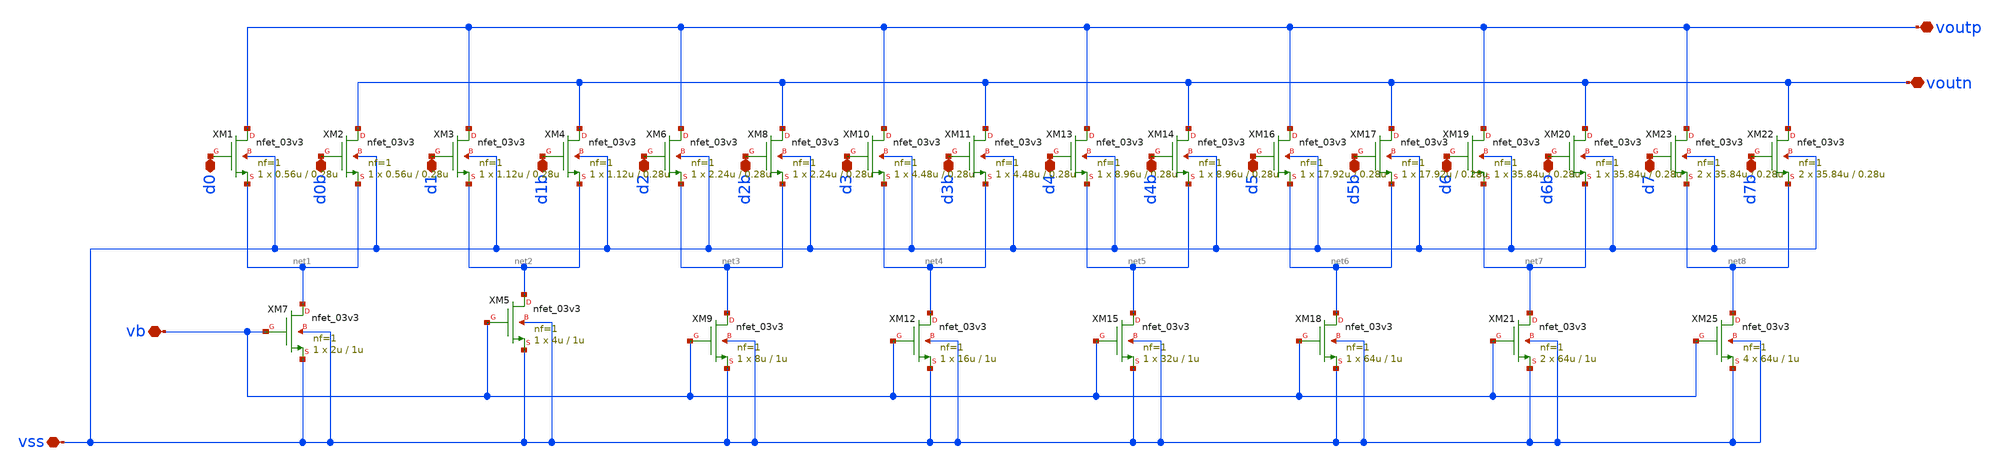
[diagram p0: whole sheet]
** sch_path: analog/dac/current_steering_dac.sch
**.subckt current_steering_dac voutp voutn d7b d7 d6b d6 d5b d5 d4b d4 d3b d3 d2b d2 d1b d1 d0b d0
*+ vb vss
*.iopin voutp
*.iopin voutn
*.iopin d7b
*.iopin d7
*.iopin d6b
*.iopin d6
*.iopin d5b
*.iopin d5
*.iopin d4b
*.iopin d4
*.iopin d3b
*.iopin d3
*.iopin d2b
*.iopin d2
*.iopin d1b
*.iopin d1
*.iopin d0b
*.iopin d0
*.iopin vb
*.iopin vss
XM1 voutp d0 net1 vss nfet_03v3 L=0.28u W=0.56u nf=1 ad='int((nf+1)/2) * W/nf * 0.18u' as='int((nf+2)/2) * W/nf * 0.18u'
+ pd='2*int((nf+1)/2) * (W/nf + 0.18u)' ps='2*int((nf+2)/2) * (W/nf + 0.18u)' nrd='0.18u / W' nrs='0.18u / W'
+ sa=0 sb=0 sd=0 m=1
XM7 net1 vb vss vss nfet_03v3 L=1u W=2u nf=1 ad='int((nf+1)/2) * W/nf * 0.18u' as='int((nf+2)/2) * W/nf * 0.18u'
+ pd='2*int((nf+1)/2) * (W/nf + 0.18u)' ps='2*int((nf+2)/2) * (W/nf + 0.18u)' nrd='0.18u / W' nrs='0.18u / W'
+ sa=0 sb=0 sd=0 m=1
XM5 net2 vb vss vss nfet_03v3 L=1u W=4u nf=1 ad='int((nf+1)/2) * W/nf * 0.18u' as='int((nf+2)/2) * W/nf * 0.18u'
+ pd='2*int((nf+1)/2) * (W/nf + 0.18u)' ps='2*int((nf+2)/2) * (W/nf + 0.18u)' nrd='0.18u / W' nrs='0.18u / W'
+ sa=0 sb=0 sd=0 m=1
XM9 net3 vb vss vss nfet_03v3 L=1u W=8u nf=1 ad='int((nf+1)/2) * W/nf * 0.18u' as='int((nf+2)/2) * W/nf * 0.18u'
+ pd='2*int((nf+1)/2) * (W/nf + 0.18u)' ps='2*int((nf+2)/2) * (W/nf + 0.18u)' nrd='0.18u / W' nrs='0.18u / W'
+ sa=0 sb=0 sd=0 m=1
XM12 net4 vb vss vss nfet_03v3 L=1u W=16u nf=1 ad='int((nf+1)/2) * W/nf * 0.18u' as='int((nf+2)/2) * W/nf * 0.18u'
+ pd='2*int((nf+1)/2) * (W/nf + 0.18u)' ps='2*int((nf+2)/2) * (W/nf + 0.18u)' nrd='0.18u / W' nrs='0.18u / W'
+ sa=0 sb=0 sd=0 m=1
XM13 voutp d4 net5 vss nfet_03v3 L=0.28u W=8.96u nf=1 ad='int((nf+1)/2) * W/nf * 0.18u' as='int((nf+2)/2) * W/nf * 0.18u'
+ pd='2*int((nf+1)/2) * (W/nf + 0.18u)' ps='2*int((nf+2)/2) * (W/nf + 0.18u)' nrd='0.18u / W' nrs='0.18u / W'
+ sa=0 sb=0 sd=0 m=1
XM15 net5 vb vss vss nfet_03v3 L=1u W=32u nf=1 ad='int((nf+1)/2) * W/nf * 0.18u' as='int((nf+2)/2) * W/nf * 0.18u'
+ pd='2*int((nf+1)/2) * (W/nf + 0.18u)' ps='2*int((nf+2)/2) * (W/nf + 0.18u)' nrd='0.18u / W' nrs='0.18u / W'
+ sa=0 sb=0 sd=0 m=1
XM16 voutp d5 net6 vss nfet_03v3 L=0.28u W=17.92u nf=1 ad='int((nf+1)/2) * W/nf * 0.18u' as='int((nf+2)/2) * W/nf * 0.18u'
+ pd='2*int((nf+1)/2) * (W/nf + 0.18u)' ps='2*int((nf+2)/2) * (W/nf + 0.18u)' nrd='0.18u / W' nrs='0.18u / W'
+ sa=0 sb=0 sd=0 m=1
XM18 net6 vb vss vss nfet_03v3 L=1u W=64u nf=1 ad='int((nf+1)/2) * W/nf * 0.18u' as='int((nf+2)/2) * W/nf * 0.18u'
+ pd='2*int((nf+1)/2) * (W/nf + 0.18u)' ps='2*int((nf+2)/2) * (W/nf + 0.18u)' nrd='0.18u / W' nrs='0.18u / W'
+ sa=0 sb=0 sd=0 m=1
XM19 voutp d6 net7 vss nfet_03v3 L=0.28u W=35.84u nf=1 ad='int((nf+1)/2) * W/nf * 0.18u' as='int((nf+2)/2) * W/nf * 0.18u'
+ pd='2*int((nf+1)/2) * (W/nf + 0.18u)' ps='2*int((nf+2)/2) * (W/nf + 0.18u)' nrd='0.18u / W' nrs='0.18u / W'
+ sa=0 sb=0 sd=0 m=1
XM21 net7 vb vss vss nfet_03v3 L=1u W=64u nf=1 ad='int((nf+1)/2) * W/nf * 0.18u' as='int((nf+2)/2) * W/nf * 0.18u'
+ pd='2*int((nf+1)/2) * (W/nf + 0.18u)' ps='2*int((nf+2)/2) * (W/nf + 0.18u)' nrd='0.18u / W' nrs='0.18u / W'
+ sa=0 sb=0 sd=0 m=2
XM23 voutp d7 net8 vss nfet_03v3 L=0.28u W=35.84u nf=1 ad='int((nf+1)/2) * W/nf * 0.18u' as='int((nf+2)/2) * W/nf * 0.18u'
+ pd='2*int((nf+1)/2) * (W/nf + 0.18u)' ps='2*int((nf+2)/2) * (W/nf + 0.18u)' nrd='0.18u / W' nrs='0.18u / W'
+ sa=0 sb=0 sd=0 m=2
XM25 net8 vb vss vss nfet_03v3 L=1u W=64u nf=1 ad='int((nf+1)/2) * W/nf * 0.18u' as='int((nf+2)/2) * W/nf * 0.18u'
+ pd='2*int((nf+1)/2) * (W/nf + 0.18u)' ps='2*int((nf+2)/2) * (W/nf + 0.18u)' nrd='0.18u / W' nrs='0.18u / W'
+ sa=0 sb=0 sd=0 m=4
XM3 voutp d1 net2 vss nfet_03v3 L=0.28u W=1.12u nf=1 ad='int((nf+1)/2) * W/nf * 0.18u' as='int((nf+2)/2) * W/nf * 0.18u'
+ pd='2*int((nf+1)/2) * (W/nf + 0.18u)' ps='2*int((nf+2)/2) * (W/nf + 0.18u)' nrd='0.18u / W' nrs='0.18u / W'
+ sa=0 sb=0 sd=0 m=1
XM6 voutp d2 net3 vss nfet_03v3 L=0.28u W=2.24u nf=1 ad='int((nf+1)/2) * W/nf * 0.18u' as='int((nf+2)/2) * W/nf * 0.18u'
+ pd='2*int((nf+1)/2) * (W/nf + 0.18u)' ps='2*int((nf+2)/2) * (W/nf + 0.18u)' nrd='0.18u / W' nrs='0.18u / W'
+ sa=0 sb=0 sd=0 m=1
XM10 voutp d3 net4 vss nfet_03v3 L=0.28u W=4.48u nf=1 ad='int((nf+1)/2) * W/nf * 0.18u' as='int((nf+2)/2) * W/nf * 0.18u'
+ pd='2*int((nf+1)/2) * (W/nf + 0.18u)' ps='2*int((nf+2)/2) * (W/nf + 0.18u)' nrd='0.18u / W' nrs='0.18u / W'
+ sa=0 sb=0 sd=0 m=1
XM2 voutn d0b net1 vss nfet_03v3 L=0.28u W=0.56u nf=1 ad='int((nf+1)/2) * W/nf * 0.18u' as='int((nf+2)/2) * W/nf * 0.18u'
+ pd='2*int((nf+1)/2) * (W/nf + 0.18u)' ps='2*int((nf+2)/2) * (W/nf + 0.18u)' nrd='0.18u / W' nrs='0.18u / W'
+ sa=0 sb=0 sd=0 m=1
XM4 voutn d1b net2 vss nfet_03v3 L=0.28u W=1.12u nf=1 ad='int((nf+1)/2) * W/nf * 0.18u' as='int((nf+2)/2) * W/nf * 0.18u'
+ pd='2*int((nf+1)/2) * (W/nf + 0.18u)' ps='2*int((nf+2)/2) * (W/nf + 0.18u)' nrd='0.18u / W' nrs='0.18u / W'
+ sa=0 sb=0 sd=0 m=1
XM8 voutn d2b net3 vss nfet_03v3 L=0.28u W=2.24u nf=1 ad='int((nf+1)/2) * W/nf * 0.18u' as='int((nf+2)/2) * W/nf * 0.18u'
+ pd='2*int((nf+1)/2) * (W/nf + 0.18u)' ps='2*int((nf+2)/2) * (W/nf + 0.18u)' nrd='0.18u / W' nrs='0.18u / W'
+ sa=0 sb=0 sd=0 m=1
XM11 voutn d3b net4 vss nfet_03v3 L=0.28u W=4.48u nf=1 ad='int((nf+1)/2) * W/nf * 0.18u' as='int((nf+2)/2) * W/nf * 0.18u'
+ pd='2*int((nf+1)/2) * (W/nf + 0.18u)' ps='2*int((nf+2)/2) * (W/nf + 0.18u)' nrd='0.18u / W' nrs='0.18u / W'
+ sa=0 sb=0 sd=0 m=1
XM14 voutn d4b net5 vss nfet_03v3 L=0.28u W=8.96u nf=1 ad='int((nf+1)/2) * W/nf * 0.18u' as='int((nf+2)/2) * W/nf * 0.18u'
+ pd='2*int((nf+1)/2) * (W/nf + 0.18u)' ps='2*int((nf+2)/2) * (W/nf + 0.18u)' nrd='0.18u / W' nrs='0.18u / W'
+ sa=0 sb=0 sd=0 m=1
XM17 voutn d5b net6 vss nfet_03v3 L=0.28u W=17.92u nf=1 ad='int((nf+1)/2) * W/nf * 0.18u' as='int((nf+2)/2) * W/nf * 0.18u'
+ pd='2*int((nf+1)/2) * (W/nf + 0.18u)' ps='2*int((nf+2)/2) * (W/nf + 0.18u)' nrd='0.18u / W' nrs='0.18u / W'
+ sa=0 sb=0 sd=0 m=1
XM20 voutn d6b net7 vss nfet_03v3 L=0.28u W=35.84u nf=1 ad='int((nf+1)/2) * W/nf * 0.18u' as='int((nf+2)/2) * W/nf * 0.18u'
+ pd='2*int((nf+1)/2) * (W/nf + 0.18u)' ps='2*int((nf+2)/2) * (W/nf + 0.18u)' nrd='0.18u / W' nrs='0.18u / W'
+ sa=0 sb=0 sd=0 m=1
XM22 voutn d7b net8 vss nfet_03v3 L=0.28u W=35.84u nf=1 ad='int((nf+1)/2) * W/nf * 0.18u' as='int((nf+2)/2) * W/nf * 0.18u'
+ pd='2*int((nf+1)/2) * (W/nf + 0.18u)' ps='2*int((nf+2)/2) * (W/nf + 0.18u)' nrd='0.18u / W' nrs='0.18u / W'
+ sa=0 sb=0 sd=0 m=2
**.ends
.end
